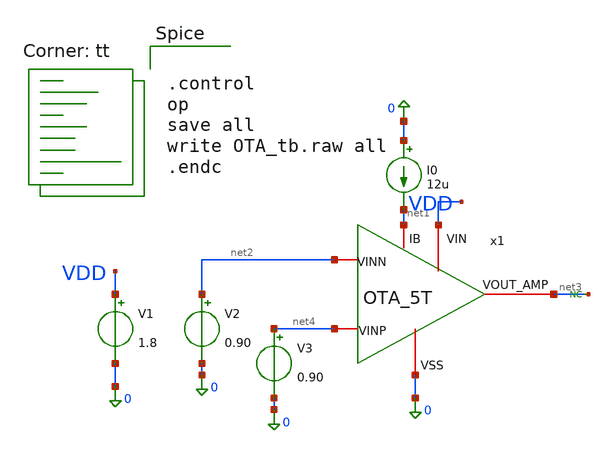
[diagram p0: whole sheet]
** sch_path: OTA_5T/OTA_tb.sch
**.subckt OTA_tb
V1 VDD 0 1.8
V2 net2 0 0.90
I0 0 net1 12u
* noconn #net3
V3 net4 0 0.90
x1 VDD net3 net2 net4 net1 0 OTA_5T
**** begin user architecture code
.lib $::SKYWATER_MODELS/sky130.lib.spice tt


.control
op
save all
write OTA_tb.raw all
.endc



.save @m.x1.xm3.msky130_fd_pr__nfet_01v8[gm]
.save @m.x1.xm4.msky130_fd_pr__nfet_01v8[gm]
.save @m.x1.xm5.msky130_fd_pr__pfet_01v8[gm]
.save @m.x1.xm6.msky130_fd_pr__pfet_01v8[gm]
.save @m.x1.xm3.msky130_fd_pr__nfet_01v8[id]
.save @m.x1.xm4.msky130_fd_pr__nfet_01v8[id]
.save @m.x1.xm5.msky130_fd_pr__pfet_01v8[id]
.save @m.x1.xm6.msky130_fd_pr__pfet_01v8[id]
.save @m.x1.xm3.msky130_fd_pr__nfet_01v8[vgs]
.save @m.x1.xm4.msky130_fd_pr__nfet_01v8[vgs]
.save @m.x1.xm5.msky130_fd_pr__pfet_01v8[vgs]
.save @m.x1.xm6.msky130_fd_pr__pfet_01v8[vgs]
.save @m.x1.xm3.msky130_fd_pr__nfet_01v8[vds]
.save @m.x1.xm4.msky130_fd_pr__nfet_01v8[vds]
.save @m.x1.xm5.msky130_fd_pr__pfet_01v8[vds]
.save @m.x1.xm6.msky130_fd_pr__pfet_01v8[vds]
.save @m.x1.xm3.msky130_fd_pr__nfet_01v8[gds]
.save @m.x1.xm4.msky130_fd_pr__nfet_01v8[gds]
.save @m.x1.xm5.msky130_fd_pr__pfet_01v8[gds]
.save @m.x1.xm6.msky130_fd_pr__pfet_01v8[gds]


**** end user architecture code
**.ends

* expanding   symbol:  /foss/designs/Curso_Semiconductores/OTA_5T/OTA_5T.sym # of pins=6
** sym_path: /foss/designs/Curso_Semiconductores/OTA_5T/OTA_5T.sym
** sch_path: /foss/designs/Curso_Semiconductores/OTA_5T/OTA_5T.sch
.subckt OTA_5T VIN VOUT_AMP VINN VINP IB VSS
*.iopin VIN
*.iopin VSS
*.iopin VOUT_AMP
*.iopin IB
*.iopin VINN
*.iopin VINP
XM1 IB IB VSS VSS sky130_fd_pr__nfet_01v8 L=1 W=2.5 nf=1 ad='int((1 + 1)/2) * 2.5 / 1 * 0.29' as='int((1 + 2)/2) * 2.5 / 1 * 0.29'
+ pd='2*int((1 + 1)/2) * (2.5 / 1 + 0.29)' ps='2*int((1 + 2)/2) * (2.5 / 1 + 0.29)' nrd='0.29 / 2.5 ' nrs='0.29 / 2.5 '
+ sa=0 sb=0 sd=0 mult=4 m=4
XM2 tail IB VSS VSS sky130_fd_pr__nfet_01v8 L=1 W=2.5 nf=1 ad='int((1 + 1)/2) * 2.5 / 1 * 0.29' as='int((1 + 2)/2) * 2.5 / 1 * 0.29'
+ pd='2*int((1 + 1)/2) * (2.5 / 1 + 0.29)' ps='2*int((1 + 2)/2) * (2.5 / 1 + 0.29)' nrd='0.29 / 2.5 ' nrs='0.29 / 2.5 '
+ sa=0 sb=0 sd=0 mult=4 m=4
XM3 net1 VINP tail VSS sky130_fd_pr__nfet_01v8 L=1 W=3 nf=1 ad='int((1 + 1)/2) * 3 / 1 * 0.29' as='int((1 + 2)/2) * 3 / 1 * 0.29'
+ pd='2*int((1 + 1)/2) * (3 / 1 + 0.29)' ps='2*int((1 + 2)/2) * (3 / 1 + 0.29)' nrd='0.29 / 3 ' nrs='0.29 / 3 '
+ sa=0 sb=0 sd=0 mult=4 m=4
XM4 VOUT_AMP VINN tail VSS sky130_fd_pr__nfet_01v8 L=1 W=3 nf=1 ad='int((1 + 1)/2) * 3 / 1 * 0.29' as='int((1 + 2)/2) * 3 / 1 * 0.29'
+ pd='2*int((1 + 1)/2) * (3 / 1 + 0.29)' ps='2*int((1 + 2)/2) * (3 / 1 + 0.29)' nrd='0.29 / 3 ' nrs='0.29 / 3 '
+ sa=0 sb=0 sd=0 mult=4 m=4
XM5 VOUT_AMP net1 VIN VIN sky130_fd_pr__pfet_01v8 L=1 W=6 nf=1 ad='int((1 + 1)/2) * 6 / 1 * 0.29' as='int((1 + 2)/2) * 6 / 1 * 0.29'
+ pd='2*int((1 + 1)/2) * (6 / 1 + 0.29)' ps='2*int((1 + 2)/2) * (6 / 1 + 0.29)' nrd='0.29 / 6 ' nrs='0.29 / 6 '
+ sa=0 sb=0 sd=0 mult=4 m=4
XM6 net1 net1 VIN VIN sky130_fd_pr__pfet_01v8 L=1 W=6 nf=1 ad='int((1 + 1)/2) * 6 / 1 * 0.29' as='int((1 + 2)/2) * 6 / 1 * 0.29'
+ pd='2*int((1 + 1)/2) * (6 / 1 + 0.29)' ps='2*int((1 + 2)/2) * (6 / 1 + 0.29)' nrd='0.29 / 6 ' nrs='0.29 / 6 '
+ sa=0 sb=0 sd=0 mult=4 m=4
XD tail VSS tail VSS sky130_fd_pr__nfet_01v8 L=0.15 W=3 nf=1 ad='int((1 + 1)/2) * 3 / 1 * 0.29' as='int((1 + 2)/2) * 3 / 1 * 0.29'
+ pd='2*int((1 + 1)/2) * (3 / 1 + 0.29)' ps='2*int((1 + 2)/2) * (3 / 1 + 0.29)' nrd='0.29 / 3 ' nrs='0.29 / 3 '
+ sa=0 sb=0 sd=0 mult=4 m=4
XM7 VIN VIN VIN VIN sky130_fd_pr__pfet_01v8 L=0.15 W=6 nf=1 ad='int((1 + 1)/2) * 6 / 1 * 0.29' as='int((1 + 2)/2) * 6 / 1 * 0.29'
+ pd='2*int((1 + 1)/2) * (6 / 1 + 0.29)' ps='2*int((1 + 2)/2) * (6 / 1 + 0.29)' nrd='0.29 / 6 ' nrs='0.29 / 6 '
+ sa=0 sb=0 sd=0 mult=4 m=4
.ends

.end
